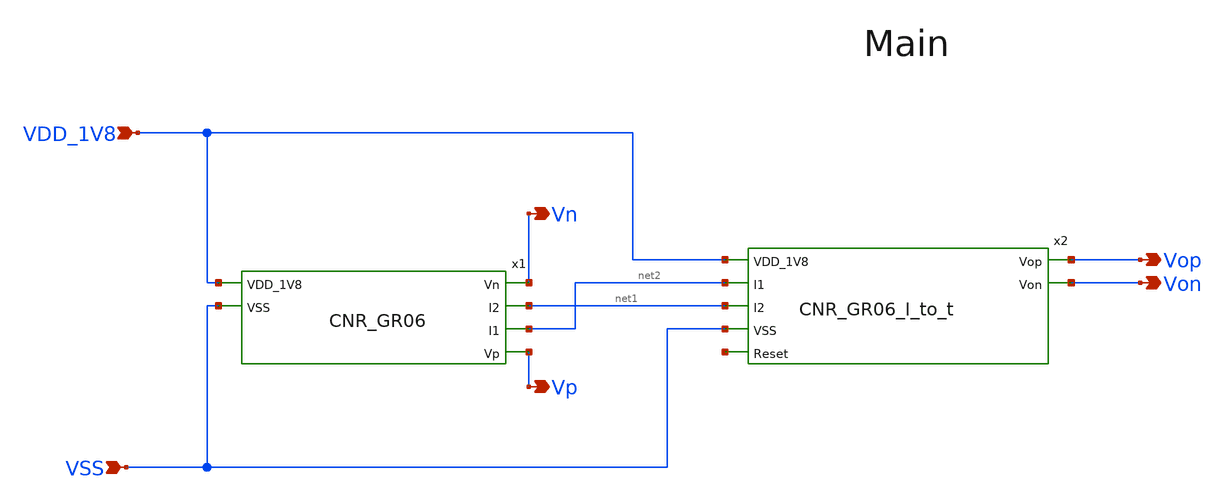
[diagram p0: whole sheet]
** sch_path: design/CNR_GR06_SKY130NM/CNR_GR06_main.sch
**.subckt CNR_GR06_main VDD_1V8 VSS Vn Vp Vop Von
*.ipin VDD_1V8
*.ipin VSS
*.opin Vn
*.opin Vp
*.opin Vop
*.opin Von
x2 VDD_1V8 Vop Von net2 net1 VSS net3 CNR_GR06_I_to_t
x1 VDD_1V8 Vn net1 net2 Vp VSS CNR_GR06
**.ends
.end
